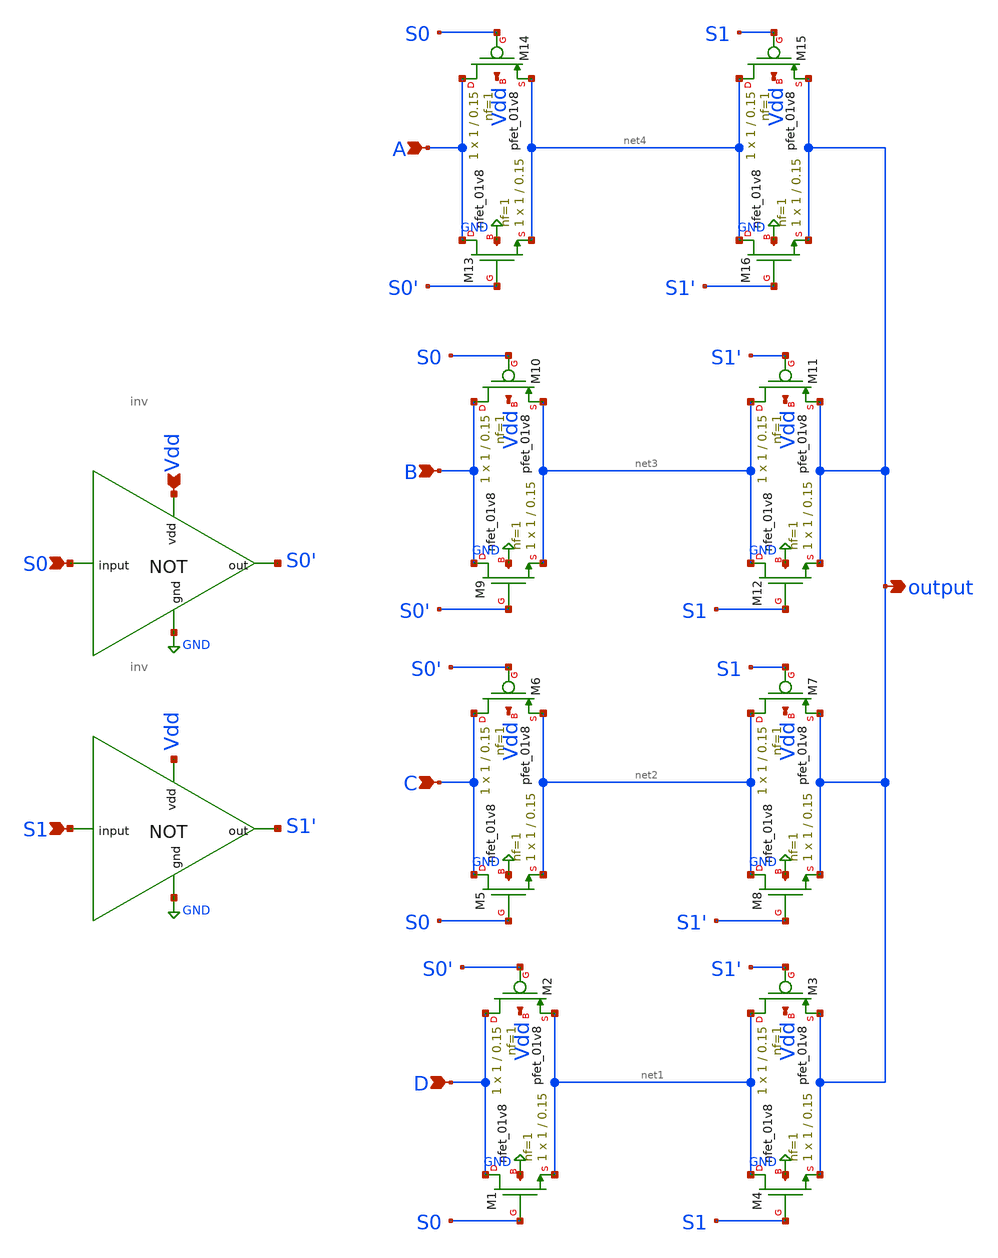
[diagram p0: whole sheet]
** sch_path: schematics/mux4to1.sch
**.subckt mux4to1 output S1 S0 A B C D Vdd
*.opin output
*.ipin S1
*.ipin S0
*.ipin A
*.ipin B
*.ipin C
*.ipin D
*.ipin Vdd
XM1 D S0 net1 GND sky130_fd_pr__nfet_01v8 L=0.15 W=1 nf=1 ad='int((1 + 1)/2) * 1 / 1 * 0.29' as='int((1 + 2)/2) * 1 / 1 * 0.29'
+ pd='2*int((1 + 1)/2) * (1 / 1 + 0.29)' ps='2*int((1 + 2)/2) * (1 / 1 + 0.29)' nrd='0.29 / 1 ' nrs='0.29 / 1 '
+ sa=0 sb=0 sd=0 mult=1 m=1
XM2 D S0' net1 Vdd sky130_fd_pr__pfet_01v8 L=0.15 W=1 nf=1 ad='int((1 + 1)/2) * 1 / 1 * 0.29' as='int((1
+ + 2)/2) * 1 / 1 * 0.29' pd='2*int((1 + 1)/2) * (1 / 1 + 0.29)' ps='2*int((1 + 2)/2) * (1 / 1 + 0.29)' nrd='0.29
+ / 1 ' nrs='0.29 / 1 ' sa=0 sb=0 sd=0 mult=1 m=1
XM3 net1 S1' output Vdd sky130_fd_pr__pfet_01v8 L=0.15 W=1 nf=1 ad='int((1 + 1)/2) * 1 / 1 * 0.29' as='int((1 + 2)/2) * 1 / 1 * 0.29'
+ pd='2*int((1 + 1)/2) * (1 / 1 + 0.29)' ps='2*int((1 + 2)/2) * (1 / 1 + 0.29)' nrd='0.29 / 1 ' nrs='0.29 / 1 '
+ sa=0 sb=0 sd=0 mult=1 m=1
XM4 net1 S1 output GND sky130_fd_pr__nfet_01v8 L=0.15 W=1 nf=1 ad='int((1 + 1)/2) * 1 / 1 * 0.29' as='int((1 + 2)/2) * 1 / 1 * 0.29'
+ pd='2*int((1 + 1)/2) * (1 / 1 + 0.29)' ps='2*int((1 + 2)/2) * (1 / 1 + 0.29)' nrd='0.29 / 1 ' nrs='0.29 / 1 '
+ sa=0 sb=0 sd=0 mult=1 m=1
XM5 C S0 net2 GND sky130_fd_pr__nfet_01v8 L=0.15 W=1 nf=1 ad='int((1 + 1)/2) * 1 / 1 * 0.29' as='int((1 + 2)/2) * 1 / 1 * 0.29'
+ pd='2*int((1 + 1)/2) * (1 / 1 + 0.29)' ps='2*int((1 + 2)/2) * (1 / 1 + 0.29)' nrd='0.29 / 1 ' nrs='0.29 / 1 '
+ sa=0 sb=0 sd=0 mult=1 m=1
XM6 C S0' net2 Vdd sky130_fd_pr__pfet_01v8 L=0.15 W=1 nf=1 ad='int((1 + 1)/2) * 1 / 1 * 0.29' as='int((1
+ + 2)/2) * 1 / 1 * 0.29' pd='2*int((1 + 1)/2) * (1 / 1 + 0.29)' ps='2*int((1 + 2)/2) * (1 / 1 + 0.29)' nrd='0.29
+ / 1 ' nrs='0.29 / 1 ' sa=0 sb=0 sd=0 mult=1 m=1
XM7 net2 S1 output Vdd sky130_fd_pr__pfet_01v8 L=0.15 W=1 nf=1 ad='int((1 + 1)/2) * 1 / 1 * 0.29' as='int((1
+ + 2)/2) * 1 / 1 * 0.29' pd='2*int((1 + 1)/2) * (1 / 1 + 0.29)' ps='2*int((1 + 2)/2) * (1 / 1 + 0.29)' nrd='0.29
+ / 1 ' nrs='0.29 / 1 ' sa=0 sb=0 sd=0 mult=1 m=1
XM8 net2 S1' output GND sky130_fd_pr__nfet_01v8 L=0.15 W=1 nf=1 ad='int((1 + 1)/2) * 1 / 1 * 0.29' as='int((1 + 2)/2) * 1 / 1 * 0.29'
+ pd='2*int((1 + 1)/2) * (1 / 1 + 0.29)' ps='2*int((1 + 2)/2) * (1 / 1 + 0.29)' nrd='0.29 / 1 ' nrs='0.29 / 1 '
+ sa=0 sb=0 sd=0 mult=1 m=1
XM9 B S0' net3 GND sky130_fd_pr__nfet_01v8 L=0.15 W=1 nf=1 ad='int((1 + 1)/2) * 1 / 1 * 0.29' as='int((1
+ + 2)/2) * 1 / 1 * 0.29' pd='2*int((1 + 1)/2) * (1 / 1 + 0.29)' ps='2*int((1 + 2)/2) * (1 / 1 + 0.29)' nrd='0.29
+ / 1 ' nrs='0.29 / 1 ' sa=0 sb=0 sd=0 mult=1 m=1
XM10 B S0 net3 Vdd sky130_fd_pr__pfet_01v8 L=0.15 W=1 nf=1 ad='int((1 + 1)/2) * 1 / 1 * 0.29' as='int((1
+ + 2)/2) * 1 / 1 * 0.29' pd='2*int((1 + 1)/2) * (1 / 1 + 0.29)' ps='2*int((1 + 2)/2) * (1 / 1 + 0.29)' nrd='0.29
+ / 1 ' nrs='0.29 / 1 ' sa=0 sb=0 sd=0 mult=1 m=1
XM11 net3 S1' output Vdd sky130_fd_pr__pfet_01v8 L=0.15 W=1 nf=1 ad='int((1 + 1)/2) * 1 / 1 * 0.29' as='int((1 + 2)/2) * 1 / 1 * 0.29'
+ pd='2*int((1 + 1)/2) * (1 / 1 + 0.29)' ps='2*int((1 + 2)/2) * (1 / 1 + 0.29)' nrd='0.29 / 1 ' nrs='0.29 / 1 '
+ sa=0 sb=0 sd=0 mult=1 m=1
XM12 net3 S1 output GND sky130_fd_pr__nfet_01v8 L=0.15 W=1 nf=1 ad='int((1 + 1)/2) * 1 / 1 * 0.29' as='int((1 + 2)/2) * 1 / 1 * 0.29'
+ pd='2*int((1 + 1)/2) * (1 / 1 + 0.29)' ps='2*int((1 + 2)/2) * (1 / 1 + 0.29)' nrd='0.29 / 1 ' nrs='0.29 / 1 '
+ sa=0 sb=0 sd=0 mult=1 m=1
XM13 A S0' net4 GND sky130_fd_pr__nfet_01v8 L=0.15 W=1 nf=1 ad='int((1 + 1)/2) * 1 / 1 * 0.29' as='int((1
+ + 2)/2) * 1 / 1 * 0.29' pd='2*int((1 + 1)/2) * (1 / 1 + 0.29)' ps='2*int((1 + 2)/2) * (1 / 1 + 0.29)' nrd='0.29
+ / 1 ' nrs='0.29 / 1 ' sa=0 sb=0 sd=0 mult=1 m=1
XM14 A S0 net4 Vdd sky130_fd_pr__pfet_01v8 L=0.15 W=1 nf=1 ad='int((1 + 1)/2) * 1 / 1 * 0.29' as='int((1
+ + 2)/2) * 1 / 1 * 0.29' pd='2*int((1 + 1)/2) * (1 / 1 + 0.29)' ps='2*int((1 + 2)/2) * (1 / 1 + 0.29)' nrd='0.29
+ / 1 ' nrs='0.29 / 1 ' sa=0 sb=0 sd=0 mult=1 m=1
XM15 net4 S1 output Vdd sky130_fd_pr__pfet_01v8 L=0.15 W=1 nf=1 ad='int((1 + 1)/2) * 1 / 1 * 0.29' as='int((1
+ + 2)/2) * 1 / 1 * 0.29' pd='2*int((1 + 1)/2) * (1 / 1 + 0.29)' ps='2*int((1 + 2)/2) * (1 / 1 + 0.29)' nrd='0.29
+ / 1 ' nrs='0.29 / 1 ' sa=0 sb=0 sd=0 mult=1 m=1
XM16 net4 S1' output GND sky130_fd_pr__nfet_01v8 L=0.15 W=1 nf=1 ad='int((1 + 1)/2) * 1 / 1 * 0.29' as='int((1 + 2)/2) * 1 / 1 * 0.29'
+ pd='2*int((1 + 1)/2) * (1 / 1 + 0.29)' ps='2*int((1 + 2)/2) * (1 / 1 + 0.29)' nrd='0.29 / 1 ' nrs='0.29 / 1 '
+ sa=0 sb=0 sd=0 mult=1 m=1
x3 S1' Vdd S1 GND inv
x1 S0' Vdd S0 GND inv
**.ends
.GLOBAL GND
.end
